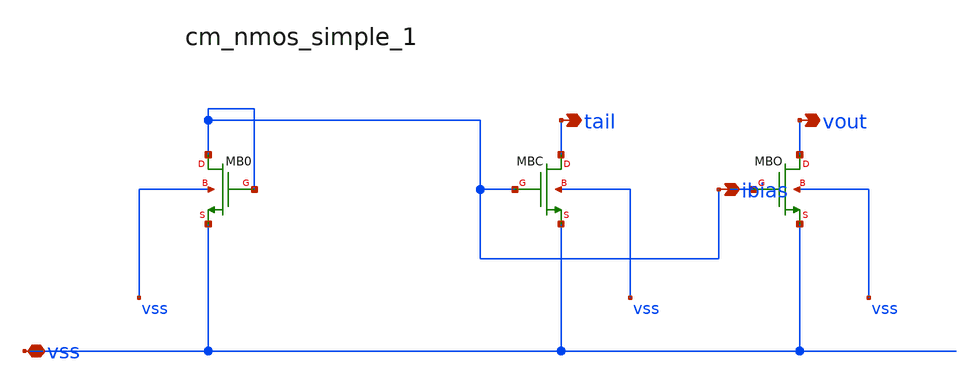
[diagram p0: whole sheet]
** sch_path: analog-db/raw/amp_033_ti_ldo_ref_selfbias/hier/blocks/cm_nmos_simple_1.sch
**.subckt cm_nmos_simple_1 vss ibias tail vout
*.iopin vss
*.opin ibias
*.opin tail
*.opin vout
XMB0 ibias ibias vss vss sg13_lv_nmos w=x_dut_xmb0_w l=x_dut_xmb0_l ng=1 m=1
XMBC tail ibias vss vss sg13_lv_nmos w=x_dut_xmbc_w l=x_dut_xmbc_l ng=1 m=x_dut_xmbc_m
XMBO vout ibias vss vss sg13_lv_nmos w=x_dut_xmbo_w l=x_dut_xmbo_l ng=1 m=x_dut_xmbo_m
**.ends
.end
